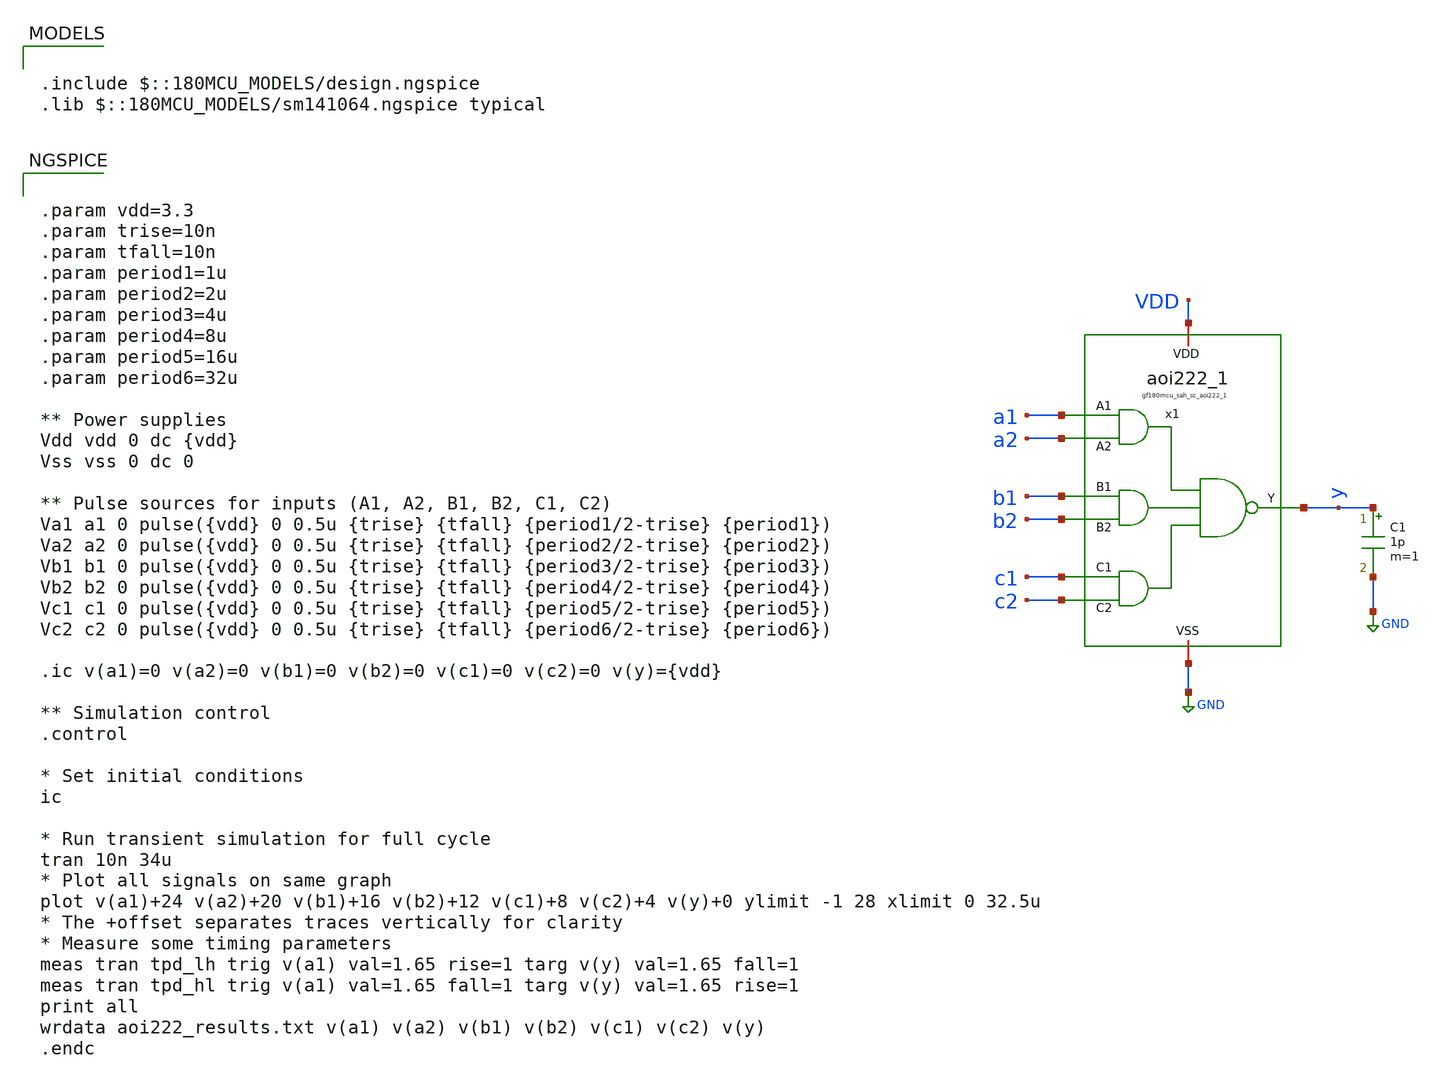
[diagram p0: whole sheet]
** sch_path: testbench/func_tb.sch
**.subckt func_tb
x1 VDD y b1 b2 GND a1 a2 c1 c2 gf180mcu_sah_sc_aoi222_1
C1 y GND 1p m=1
**** begin user architecture code


.param vdd=3.3
.param trise=10n
.param tfall=10n
.param period1=1u
.param period2=2u
.param period3=4u
.param period4=8u
.param period5=16u
.param period6=32u

** Power supplies
Vdd vdd 0 dc {vdd}
Vss vss 0 dc 0

** Pulse sources for inputs (A1, A2, B1, B2, C1, C2)
Va1 a1 0 pulse({vdd} 0 0.5u {trise} {tfall} {period1/2-trise} {period1})
Va2 a2 0 pulse({vdd} 0 0.5u {trise} {tfall} {period2/2-trise} {period2})
Vb1 b1 0 pulse({vdd} 0 0.5u {trise} {tfall} {period3/2-trise} {period3})
Vb2 b2 0 pulse({vdd} 0 0.5u {trise} {tfall} {period4/2-trise} {period4})
Vc1 c1 0 pulse({vdd} 0 0.5u {trise} {tfall} {period5/2-trise} {period5})
Vc2 c2 0 pulse({vdd} 0 0.5u {trise} {tfall} {period6/2-trise} {period6})

.ic v(a1)=0 v(a2)=0 v(b1)=0 v(b2)=0 v(c1)=0 v(c2)=0 v(y)={vdd}

** Simulation control
.control

* Set initial conditions
ic

* Run transient simulation for full cycle
tran 10n 34u
* Plot all signals on same graph
plot v(a1)+24 v(a2)+20 v(b1)+16 v(b2)+12 v(c1)+8 v(c2)+4 v(y)+0 ylimit -1 28 xlimit 0 32.5u
* The +offset separates traces vertically for clarity
* Measure some timing parameters
meas tran tpd_lh trig v(a1) val=1.65 rise=1 targ v(y) val=1.65 fall=1
meas tran tpd_hl trig v(a1) val=1.65 fall=1 targ v(y) val=1.65 rise=1
print all
wrdata aoi222_results.txt v(a1) v(a2) v(b1) v(b2) v(c1) v(c2) v(y)
.endc



.include $::180MCU_MODELS/design.ngspice
.lib $::180MCU_MODELS/sm141064.ngspice typical

**** end user architecture code
**.ends

* expanding   symbol:
*+  /headless/sscs/globalfoundries-pdk-libs-gf180mcu_sah_sc/cells/aoi222/gf180mcu_sah_sc_aoi222_1.sym # of pins=9
** sym_path: globalfoundries-pdk-libs-gf180mcu_sah_sc/cells/aoi222/gf180mcu_sah_sc_aoi222_1.sym
** sch_path: globalfoundries-pdk-libs-gf180mcu_sah_sc/cells/aoi222/gf180mcu_sah_sc_aoi222_1.sch
.subckt gf180mcu_sah_sc_aoi222_1 VDD Y B1 B2 VSS A1 A2 C1 C2
*.ipin A1
*.opin Y
*.ipin B1
*.ipin C1
*.iopin VDD
*.ipin B2
*.ipin C2
*.ipin A2
*.iopin VSS
XA2N Y A2 net1 VSS nfet_03v3 L=0.3u W=0.85u nf=1 ad='int((nf+1)/2) * W/nf * 0.18u' as='int((nf+2)/2) * W/nf * 0.18u'
+ pd='2*int((nf+1)/2) * (W/nf + 0.18u)' ps='2*int((nf+2)/2) * (W/nf + 0.18u)' nrd='0.18u / W' nrs='0.18u / W'
+ sa=0 sb=0 sd=0 m=1
XA1N net1 A1 VSS VSS nfet_03v3 L=0.3u W=0.85u nf=1 ad='int((nf+1)/2) * W/nf * 0.18u' as='int((nf+2)/2) * W/nf * 0.18u'
+ pd='2*int((nf+1)/2) * (W/nf + 0.18u)' ps='2*int((nf+2)/2) * (W/nf + 0.18u)' nrd='0.18u / W' nrs='0.18u / W'
+ sa=0 sb=0 sd=0 m=1
XA1P net5 A1 VDD VDD pfet_03v3 L=0.3u W=1.7u nf=1 ad='int((nf+1)/2) * W/nf * 0.18u' as='int((nf+2)/2) * W/nf * 0.18u'
+ pd='2*int((nf+1)/2) * (W/nf + 0.18u)' ps='2*int((nf+2)/2) * (W/nf + 0.18u)' nrd='0.18u / W' nrs='0.18u / W'
+ sa=0 sb=0 sd=0 m=1
XA2P net5 A2 VDD VDD pfet_03v3 L=0.3u W=1.7u nf=1 ad='int((nf+1)/2) * W/nf * 0.18u' as='int((nf+2)/2) * W/nf * 0.18u'
+ pd='2*int((nf+1)/2) * (W/nf + 0.18u)' ps='2*int((nf+2)/2) * (W/nf + 0.18u)' nrd='0.18u / W' nrs='0.18u / W'
+ sa=0 sb=0 sd=0 m=1
XB2N Y B2 net2 VSS nfet_03v3 L=0.3u W=0.85u nf=1 ad='int((nf+1)/2) * W/nf * 0.18u' as='int((nf+2)/2) * W/nf * 0.18u'
+ pd='2*int((nf+1)/2) * (W/nf + 0.18u)' ps='2*int((nf+2)/2) * (W/nf + 0.18u)' nrd='0.18u / W' nrs='0.18u / W'
+ sa=0 sb=0 sd=0 m=1
XB1N net2 B1 VSS VSS nfet_03v3 L=0.3u W=0.85u nf=1 ad='int((nf+1)/2) * W/nf * 0.18u' as='int((nf+2)/2) * W/nf * 0.18u'
+ pd='2*int((nf+1)/2) * (W/nf + 0.18u)' ps='2*int((nf+2)/2) * (W/nf + 0.18u)' nrd='0.18u / W' nrs='0.18u / W'
+ sa=0 sb=0 sd=0 m=1
XB1P net4 B1 net5 VDD pfet_03v3 L=0.3u W=1.7u nf=1 ad='int((nf+1)/2) * W/nf * 0.18u' as='int((nf+2)/2) * W/nf * 0.18u'
+ pd='2*int((nf+1)/2) * (W/nf + 0.18u)' ps='2*int((nf+2)/2) * (W/nf + 0.18u)' nrd='0.18u / W' nrs='0.18u / W'
+ sa=0 sb=0 sd=0 m=1
XB2P net4 B2 net5 VDD pfet_03v3 L=0.3u W=1.7u nf=1 ad='int((nf+1)/2) * W/nf * 0.18u' as='int((nf+2)/2) * W/nf * 0.18u'
+ pd='2*int((nf+1)/2) * (W/nf + 0.18u)' ps='2*int((nf+2)/2) * (W/nf + 0.18u)' nrd='0.18u / W' nrs='0.18u / W'
+ sa=0 sb=0 sd=0 m=1
XC2N Y C2 net3 VSS nfet_03v3 L=0.3u W=0.85u nf=1 ad='int((nf+1)/2) * W/nf * 0.18u' as='int((nf+2)/2) * W/nf * 0.18u'
+ pd='2*int((nf+1)/2) * (W/nf + 0.18u)' ps='2*int((nf+2)/2) * (W/nf + 0.18u)' nrd='0.18u / W' nrs='0.18u / W'
+ sa=0 sb=0 sd=0 m=1
XC1N net3 C1 VSS VSS nfet_03v3 L=0.3u W=0.85u nf=1 ad='int((nf+1)/2) * W/nf * 0.18u' as='int((nf+2)/2) * W/nf * 0.18u'
+ pd='2*int((nf+1)/2) * (W/nf + 0.18u)' ps='2*int((nf+2)/2) * (W/nf + 0.18u)' nrd='0.18u / W' nrs='0.18u / W'
+ sa=0 sb=0 sd=0 m=1
XC1P Y C1 net4 VDD pfet_03v3 L=0.3u W=1.7u nf=1 ad='int((nf+1)/2) * W/nf * 0.18u' as='int((nf+2)/2) * W/nf * 0.18u'
+ pd='2*int((nf+1)/2) * (W/nf + 0.18u)' ps='2*int((nf+2)/2) * (W/nf + 0.18u)' nrd='0.18u / W' nrs='0.18u / W'
+ sa=0 sb=0 sd=0 m=1
XC2P Y C2 net4 VDD pfet_03v3 L=0.3u W=1.7u nf=1 ad='int((nf+1)/2) * W/nf * 0.18u' as='int((nf+2)/2) * W/nf * 0.18u'
+ pd='2*int((nf+1)/2) * (W/nf + 0.18u)' ps='2*int((nf+2)/2) * (W/nf + 0.18u)' nrd='0.18u / W' nrs='0.18u / W'
+ sa=0 sb=0 sd=0 m=1
.ends

.GLOBAL GND
.end
